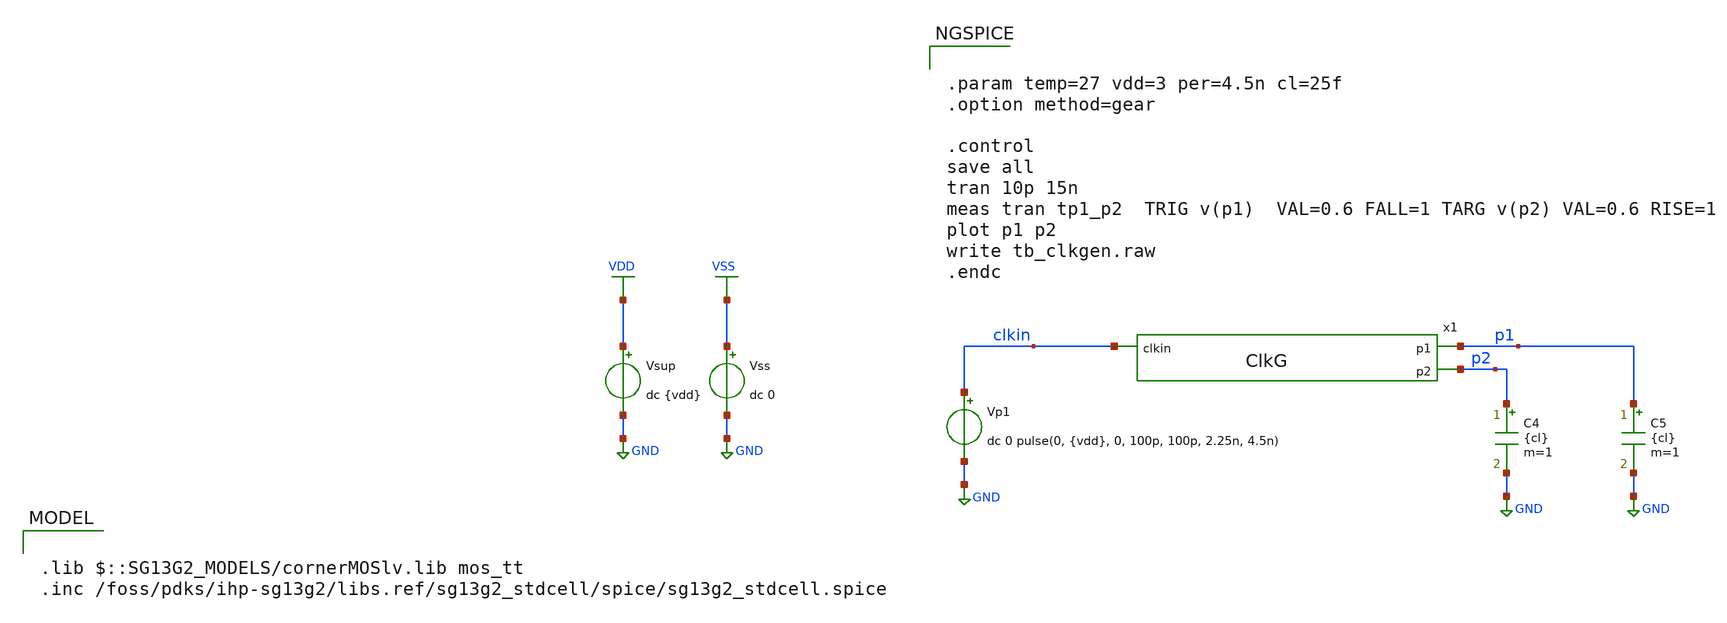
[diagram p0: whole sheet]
** sch_path: DSM_1storder/Schematic_Level/xschem/tb_ClkG.sch
* IHP-GmbH/IHP-Open-PDK/ihp-sg13g2/libs.tech/xschem/sg13g2_stdcells/sg13g2_inv_2.sch:
* Copyright 2023 IHP PDK Authors
* Licensed under the Apache License, Version 2.0 (the "License");
**.subckt tb_ClkG
Vsup VDD GND dc {vdd}
Vss VSS GND dc 0
Vp1 clkin GND dc 0 pulse(0, {vdd}, 0, 100p, 100p, 2.25n, 4.5n)
C4 p2 GND {cl} m=1
C5 p1 GND {cl} m=1
x1 clkin p1 p2 ClkG
**** begin user architecture code


.param temp=27 vdd=3 per=4.5n cl=25f
.option method=gear

.control
save all
tran 10p 15n
meas tran tp1_p2  TRIG v(p1)  VAL=0.6 FALL=1 TARG v(p2) VAL=0.6 RISE=1
plot p1 p2
write tb_clkgen.raw
.endc



.lib $::SG13G2_MODELS/cornerMOSlv.lib mos_tt
.inc /foss/pdks/ihp-sg13g2/libs.ref/sg13g2_stdcell/spice/sg13g2_stdcell.spice

**** end user architecture code
**.ends

* expanding   symbol:  ClkG.sym # of pins=3
** sym_path: DSM_1storder/Schematic_Level/xschem/ClkG.sym
** sch_path: DSM_1storder/Schematic_Level/xschem/ClkG.sch
.subckt ClkG clkin p1 p2
*.ipin clkin
*.opin p1
*.opin p2
xn1 net2 clkin net1 VDD VSS sg13g2_nand2_2
xi2 clkinb clkin VDD VSS sg13g2_inv_2
xn2 net1 net2 clkinb VDD VSS sg13g2_nand2_2
xi3 p1 net2 VDD VSS sg13g2_inv_4
xi4 p2 net1 VDD VSS sg13g2_inv_4
.ends


* expanding   symbol:  sg13g2_stdcells/sg13g2_nand2_2.sym # of pins=3
** sym_path: sg13g2_stdcells/sg13g2_nand2_2.sym
** sch_path: sg13g2_stdcells/sg13g2_nand2_2.sch
.subckt sg13g2_nand2_2 Y A B VDD VSS
*.iopin VDD
*.iopin VSS
*.opin Y
*.ipin B
*.ipin A
XM1 Y A net1 VSS sg13_lv_nmos w=1.44u l=130.00n ng=2 m=1 mm_ok=1
XM2 net1 B VSS VSS sg13_lv_nmos w=1.44u l=130.00n ng=2 m=1 mm_ok=1
XM3 Y A VDD VDD sg13_lv_pmos w=2.24u l=130.00n ng=2 m=1 mm_ok=1
XM4 Y B VDD VDD sg13_lv_pmos w=2.24u l=130.00n ng=2 m=1 mm_ok=1
.ends


* expanding   symbol:  sg13g2_stdcells/sg13g2_inv_2.sym # of pins=2
** sym_path: sg13g2_stdcells/sg13g2_inv_2.sym
** sch_path: sg13g2_stdcells/sg13g2_inv_2.sch
.subckt sg13g2_inv_2 Y A VDD VSS
*.opin Y
*.ipin A
*.iopin VDD
*.iopin VSS
XM1 Y A VSS VSS sg13_lv_nmos w=1.48u l=130.00n ng=2 m=1 mm_ok=1
XM2 Y A VDD VDD sg13_lv_pmos w=2.24u l=130.00n ng=2 m=1 mm_ok=1
.ends


* expanding   symbol:  sg13g2_stdcells/sg13g2_inv_4.sym # of pins=2
** sym_path: sg13g2_stdcells/sg13g2_inv_4.sym
** sch_path: sg13g2_stdcells/sg13g2_inv_4.sch
.subckt sg13g2_inv_4 Y A VDD VSS
*.ipin A
*.opin Y
*.iopin VDD
*.iopin VSS
XM1 Y A VSS VSS sg13_lv_nmos w=2.96u l=130.00n ng=4 m=1 mm_ok=1
XM2 Y A VDD VDD sg13_lv_pmos w=4.48u l=130.00n ng=4 m=1 mm_ok=1
.ends

.GLOBAL GND
.GLOBAL VDD
.GLOBAL VSS
.end
